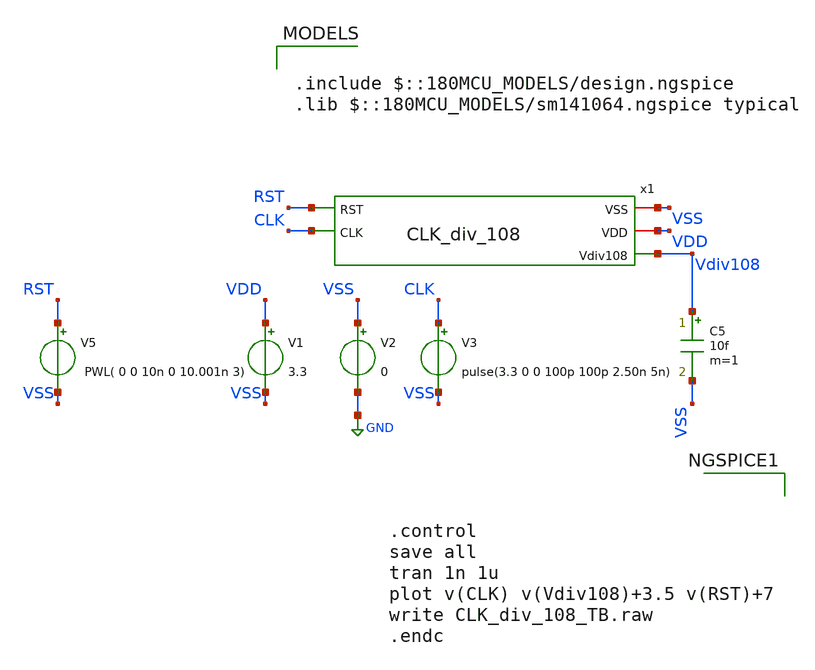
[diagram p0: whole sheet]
** sch_path: Clock_Generator_PAKISTAN_02/xschem/CLK_div_108_TB.sch
**.subckt CLK_div_108_TB
V1 VDD VSS 3.3
V2 VSS GND 0
V3 CLK VSS pulse(3.3 0 0 100p 100p 2.50n 5n)
C5 Vdiv108 VSS 10f m=1
V5 RST VSS PWL( 0 0 10n 0 10.001n 3)
x1 VSS VDD RST Vdiv108 CLK CLK_div_108
**** begin user architecture code

.include $::180MCU_MODELS/design.ngspice
.lib $::180MCU_MODELS/sm141064.ngspice typical




.control
save all
tran 1n 1u
plot v(CLK) v(Vdiv108)+3.5 v(RST)+7
write CLK_div_108_TB.raw
.endc


**** end user architecture code
**.ends
.GLOBAL GND
.end
